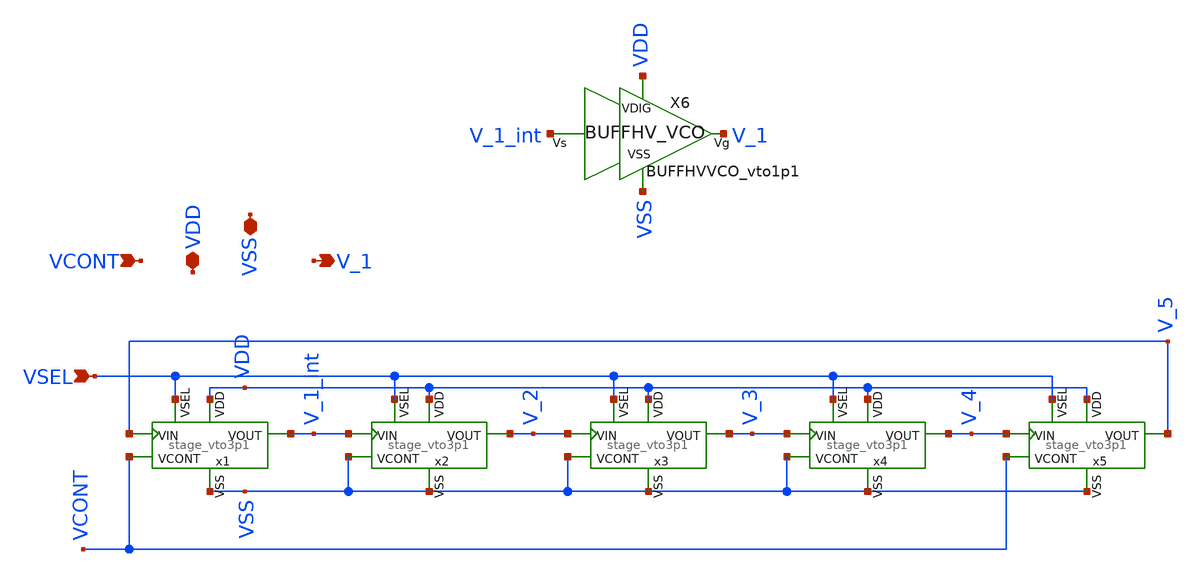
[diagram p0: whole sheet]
** sch_path: ChipUSM_AnalogTrack24/VCO/VCO_vto3p1.sch
**.subckt VCO_vto3p1 VCONT VDD VSS V_1 VSEL
*.ipin VCONT
*.iopin VDD
*.iopin VSS
*.opin V_1
*.ipin VSEL
x1 VDD VCONT V_1_int V_5 VSS VSEL stage_vto3p1
x2 VDD VSS V_2 V_1_int VSS VSEL stage_vto3p1
x3 VDD VSS V_3 V_2 VSS VSEL stage_vto3p1
x4 VDD VSS V_4 V_3 VSS VSEL stage_vto3p1
x5 VDD VCONT V_5 V_4 VSS VSEL stage_vto3p1
X6 V_1_int V_1 VDD VSS BUFFHVVCO_vto1p1
**.ends

* expanding   symbol:  ../VCO/stage_vto3p1.sym # of pins=6
** sym_path: ChipUSM_AnalogTrack24/VCO/stage_vto3p1.sym
** sch_path: ChipUSM_AnalogTrack24/VCO/stage_vto3p1.sch
.subckt stage_vto3p1 VDD VCONT VOUT VIN VSS VSEL
*.ipin VIN
*.opin VOUT
*.iopin VDD
*.iopin VSS
*.ipin VCONT
*.ipin VSEL
XM9 VSS net4 net4 VSS sg13_hv_nmos w=5u l=0.5u ng=1 m=1 mm_ok=1
XM3 VSS net4 net3 VSS sg13_hv_nmos w=5u l=0.5u ng=1 m=1 mm_ok=1
XM5 VSS net4 net2 VSS sg13_hv_nmos w=3u l=0.5u ng=1 m=1 mm_ok=1
XM8 net4 VCONT VDD VDD sg13_hv_pmos w=0.4u l=7u ng=1 m=1 mm_ok=1
XM4 net3 net3 VDD VDD sg13_hv_pmos w=8u l=4u ng=1 m=1 mm_ok=1
XM6 net1 net3 VDD VDD sg13_hv_pmos w=5u l=4u ng=1 m=1 mm_ok=1
XM2 VOUT VIN net1 VDD sg13_hv_pmos w=5u l=5u ng=1 m=1 mm_ok=1
XM1 net2 VIN VOUT VSS sg13_hv_nmos w=2u l=5u ng=1 m=1 mm_ok=1
XM7 net4 VSEL VDD VDD sg13_hv_pmos w=0.4u l=7u ng=1 m=9 mm_ok=1
.ends


* expanding   symbol:  ../BUFFHVVCO/BUFFHVVCO_vto1p1.sym # of pins=4
** sym_path: ChipUSM_AnalogTrack24/BUFFHVVCO/BUFFHVVCO_vto1p1.sym
** sch_path: ChipUSM_AnalogTrack24/BUFFHVVCO/BUFFHVVCO_vto1p1.sch
.subckt BUFFHVVCO_vto1p1 Vs Vg VDIG VSS
*.iopin VDIG
*.ipin Vs
*.opin Vg
*.iopin VSS
XMD5 net1 Vs VDIG VDIG sg13_hv_pmos w=1u l=0.45u ng=1 m=2 mm_ok=1
XMD6 VSS Vs net1 VSS sg13_hv_nmos w=1u l=0.45u ng=1 m=1 mm_ok=1
XMD1 Vg net1 VDIG VDIG sg13_hv_pmos w=1u l=0.45u ng=1 m=4 mm_ok=1
XMD2 VSS net1 Vg VSS sg13_hv_nmos w=1u l=0.45u ng=1 m=2 mm_ok=1
.ends

.end
